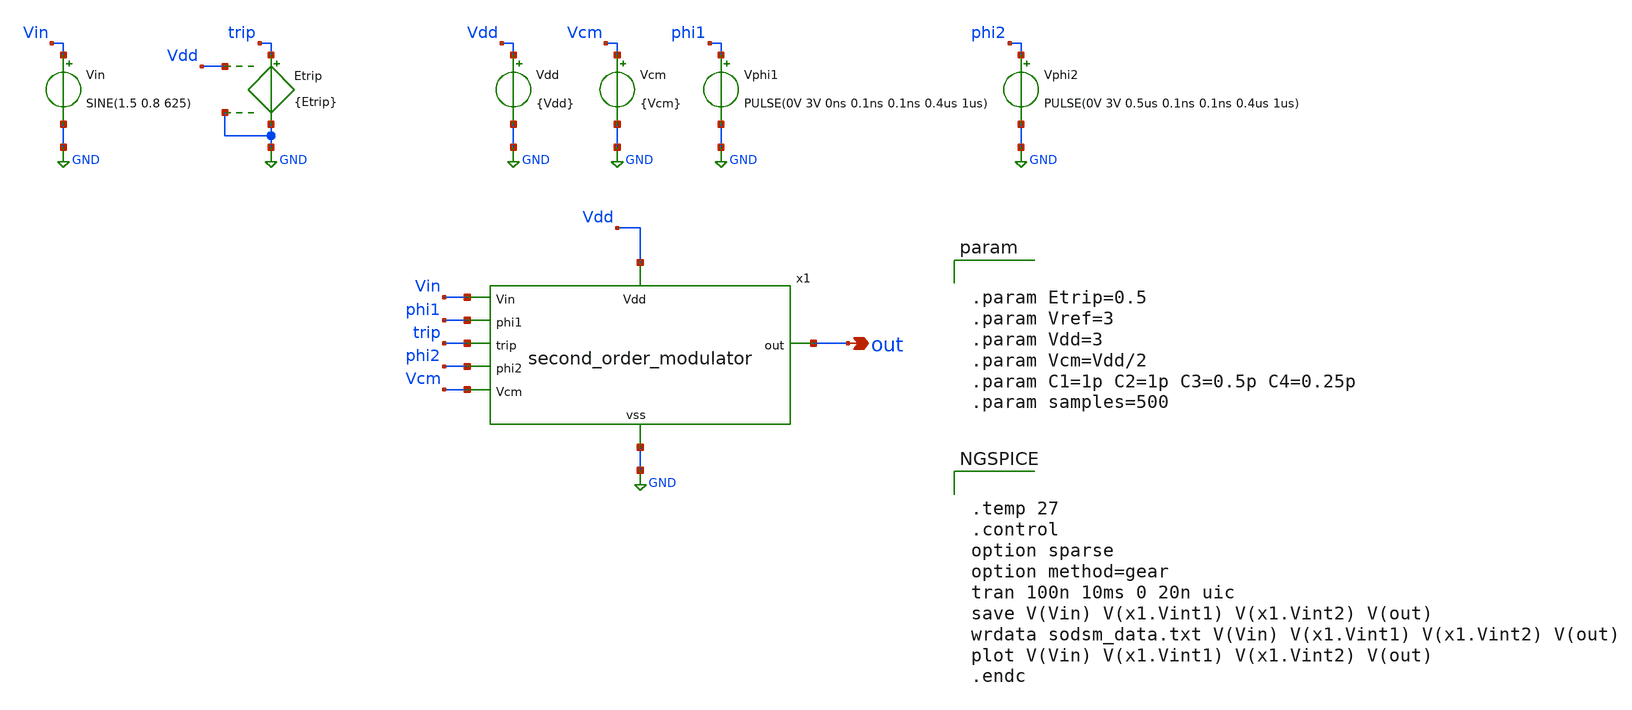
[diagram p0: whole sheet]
** sch_path: 2_ideal_circuits/second_order_delta_sigma_adc_single_ended.sch
**.subckt second_order_delta_sigma_adc_single_ended out
*.opin out
x1 Vin out phi1 trip phi2 Vcm Vdd GND second_order_modulator
Vin Vin GND SINE(1.5 0.8 625)
Vdd Vdd GND {Vdd}
Vcm Vcm GND {Vcm}
Vphi1 phi1 GND PULSE(0V 3V 0ns 0.1ns 0.1ns 0.4us 1us)
Vphi2 phi2 GND PULSE(0V 3V 0.5us 0.1ns 0.1ns 0.4us 1us)
Etrip trip GND Vdd GND {Etrip}
**** begin user architecture code


.param Etrip=0.5
.param Vref=3
.param Vdd=3
.param Vcm=Vdd/2
.param C1=1p C2=1p C3=0.5p C4=0.25p
.param samples=500




.temp 27
.control
option sparse
option method=gear
tran 100n 10ms 0 20n uic
save V(Vin) V(x1.Vint1) V(x1.Vint2) V(out)
wrdata sodsm_data.txt V(Vin) V(x1.Vint1) V(x1.Vint2) V(out)
plot V(Vin) V(x1.Vint1) V(x1.Vint2) V(out)
.endc


**** end user architecture code
**.ends

* expanding   symbol:  second_order_modulator.sym # of pins=8
** sym_path: 2_ideal_circuits/second_order_modulator.sym
** sch_path: 2_ideal_circuits/second_order_modulator.sch
.subckt second_order_modulator Vin out phi1 trip phi2 Vcm Vdd vss
*.ipin Vin
*.ipin phi1
*.ipin trip
*.ipin phi2
*.ipin Vcm
*.ipin Vdd
*.iopin vss
*.opin out
S1 Vin net1 phi1 trip SW1
S2 net1 Vfb phi2 trip SW1
S3 diff net2 phi2 trip SW1
S4 net2 Vcm phi1 trip SW1
x1 Vcm diff Vint1 ideal_opamp
C2 diff Vint1 {C2} m=1
C1 net1 net2 {C1} m=1
S5 Vint1 net3 phi2 trip SW1
S6 net3 Vfb phi1 trip SW1
S7 diff2 net4 phi1 trip SW1
S8 net4 Vcm phi2 trip SW1
x4 Vcm diff2 Vint2 ideal_opamp
C3 diff2 Vint2 {C2} m=1
C4 net3 net4 {C1} m=1
x3 Vdd out Vint2 Vcm phi1 ideal_comparator
x5 Vfb out vss Vdd ideal_inverter
.ends


* expanding   symbol:  ideal_opamp.sym # of pins=3
** sym_path: ideal_opamp.sym
** sch_path: ideal_opamp.sch
.subckt ideal_opamp inp inn out
*.opin out
*.ipin inp
*.ipin inn
E1 out GND inp inn 1Meg
R1 out GND 100Meg m=1
.ends


* expanding   symbol:  ideal_comparator.sym # of pins=5
** sym_path: 2_ideal_circuits/ideal_comparator.sym
** sch_path: 2_ideal_circuits/ideal_comparator.sch
.subckt ideal_comparator Vdd Vout Vinn Vinp clk
*.ipin Vinp
*.ipin Vinn
*.opin Vout
*.iopin Vdd
*.iopin clk
E1 diff GND Vinp Vinn 1
S1 diff sample tp clk SW1
E2 net1 GND sample GND 1
C1 sample GND 100p m=1
S2 net1 hold clk tp SW1
C2 hold GND 100p m=1
B1 Vout GND V={v(hold)>0?v(Vdd):0}
Etp tp GND Vdd GND 0.5
**** begin user architecture code


.ic v(hold)=1 v(sample)=1


**** end user architecture code
.ends


* expanding   symbol:  ideal_inverter.sym # of pins=4
** sym_path: 2_ideal_circuits/ideal_inverter.sym
** sch_path: 2_ideal_circuits/ideal_inverter.sch
.subckt ideal_inverter out in vss vdd
*.iopin vdd
*.ipin in
*.opin out
*.iopin vss
B1 out GND V={v(in)>v(vdd)/2?v(vss):v(vdd)}
* noconn vdd
* noconn in
* noconn vss
.ends

.GLOBAL GND
**** begin user architecture code
.MODEL SW1 SW( VT=0.9 VH=0.01 RON=0.01 ROFF=10G )
**** end user architecture code
.end
